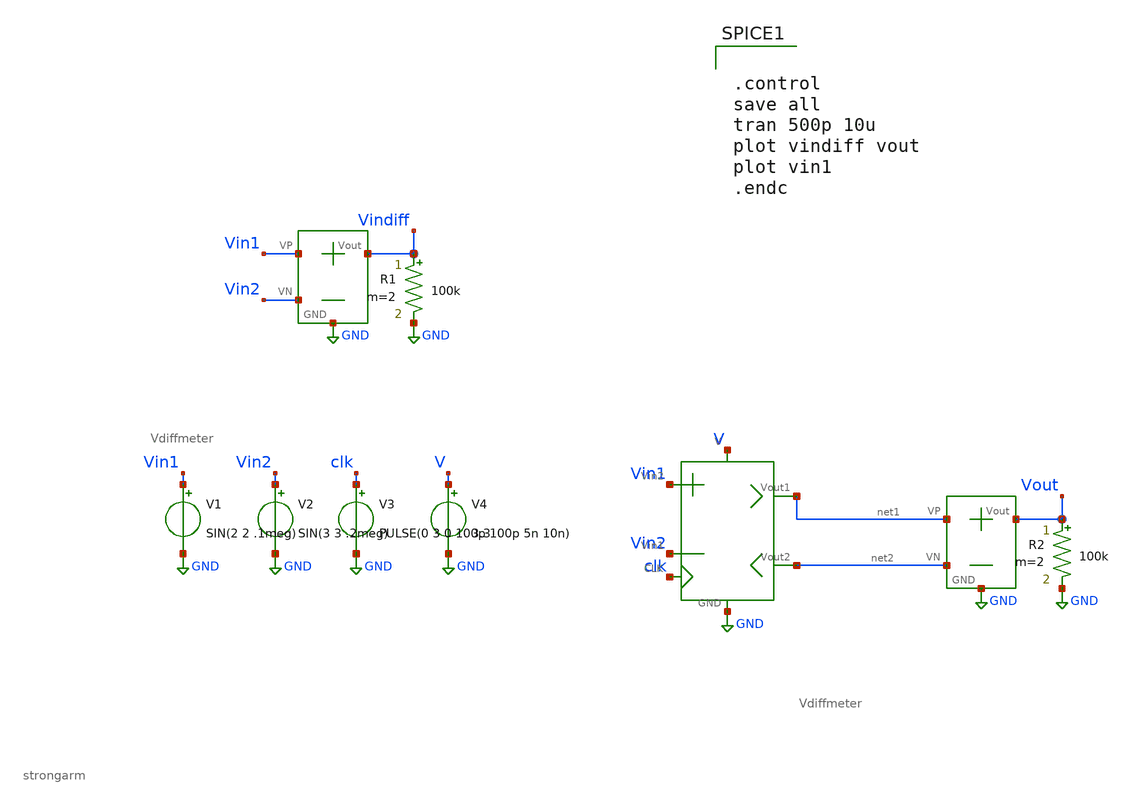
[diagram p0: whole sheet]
** sch_path: SAR_ADC/xschem/test/strongarm_tb/sin_100k-sin_200k__tb.sch
**.subckt sin_100k-sin_200k__tb
V1 Vin1 GND SIN(2 2 .1meg)
V2 Vin2 GND SIN(3 3 .2meg)
V3 clk GND PULSE(0 3 0 100p 100p 5n 10n)
V4 V GND 3.3
X2 Vin1 Vin2 Vindiff GND Vdiffmeter
R1 Vindiff GND 100k m=2
X3 net1 net2 Vout GND Vdiffmeter
R2 Vout GND 100k m=2
X1 V GND Vin2 Vin1 clk net1 net2 strongarm
**** begin user architecture code


.control
save all
tran 500p 10u
plot vindiff vout
plot vin1
.endc


.include /foss/pdks/gf180mcuC/libs.tech/ngspice/design.ngspice
.lib /foss/pdks/gf180mcuC/libs.tech/ngspice/sm141064.ngspice typical

**** end user architecture code
**.ends
.GLOBAL GND
.end
